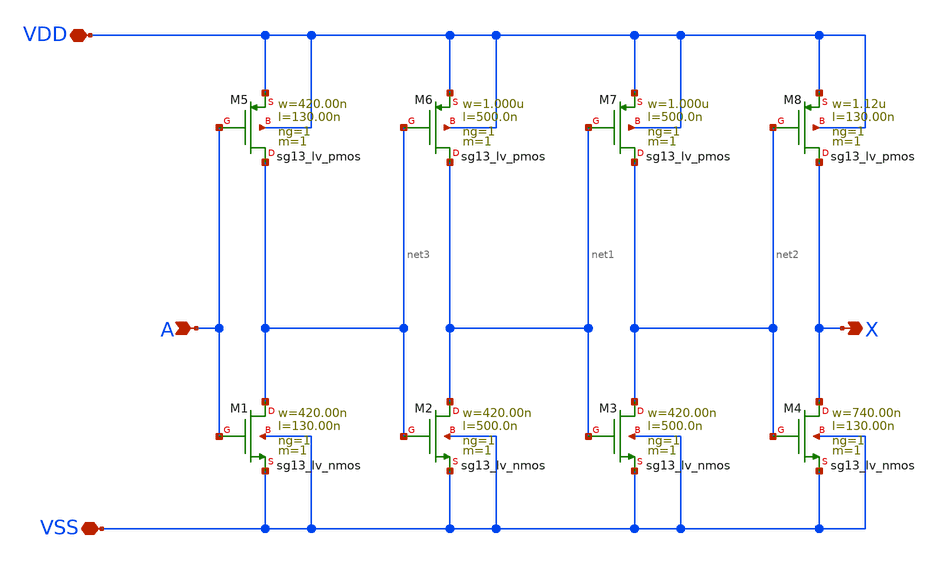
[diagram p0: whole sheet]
** sch_path: ihp-sg13g2/libs.tech/xschem/sg13g2_stdcells/sg13g2_dlygate4sd3_1.sch
**.subckt sg13g2_dlygate4sd3_1 A X VDD VSS
*.ipin A
*.opin X
*.iopin VDD
*.iopin VSS
XM1 net3 A VSS VSS sg13_lv_nmos w=420.00n l=130.00n ng=1 m=1 mm_ok=1
XM2 net1 net3 VSS VSS sg13_lv_nmos w=420.00n l=500.0n ng=1 m=1 mm_ok=1
XM3 net2 net1 VSS VSS sg13_lv_nmos w=420.00n l=500.0n ng=1 m=1 mm_ok=1
XM4 X net2 VSS VSS sg13_lv_nmos w=740.00n l=130.00n ng=1 m=1 mm_ok=1
XM5 net3 A VDD VDD sg13_lv_pmos w=420.00n l=130.00n ng=1 m=1 mm_ok=1
XM6 net1 net3 VDD VDD sg13_lv_pmos w=1.000u l=500.0n ng=1 m=1 mm_ok=1
XM7 net2 net1 VDD VDD sg13_lv_pmos w=1.000u l=500.0n ng=1 m=1 mm_ok=1
XM8 X net2 VDD VDD sg13_lv_pmos w=1.12u l=130.00n ng=1 m=1 mm_ok=1
**.ends
.end
